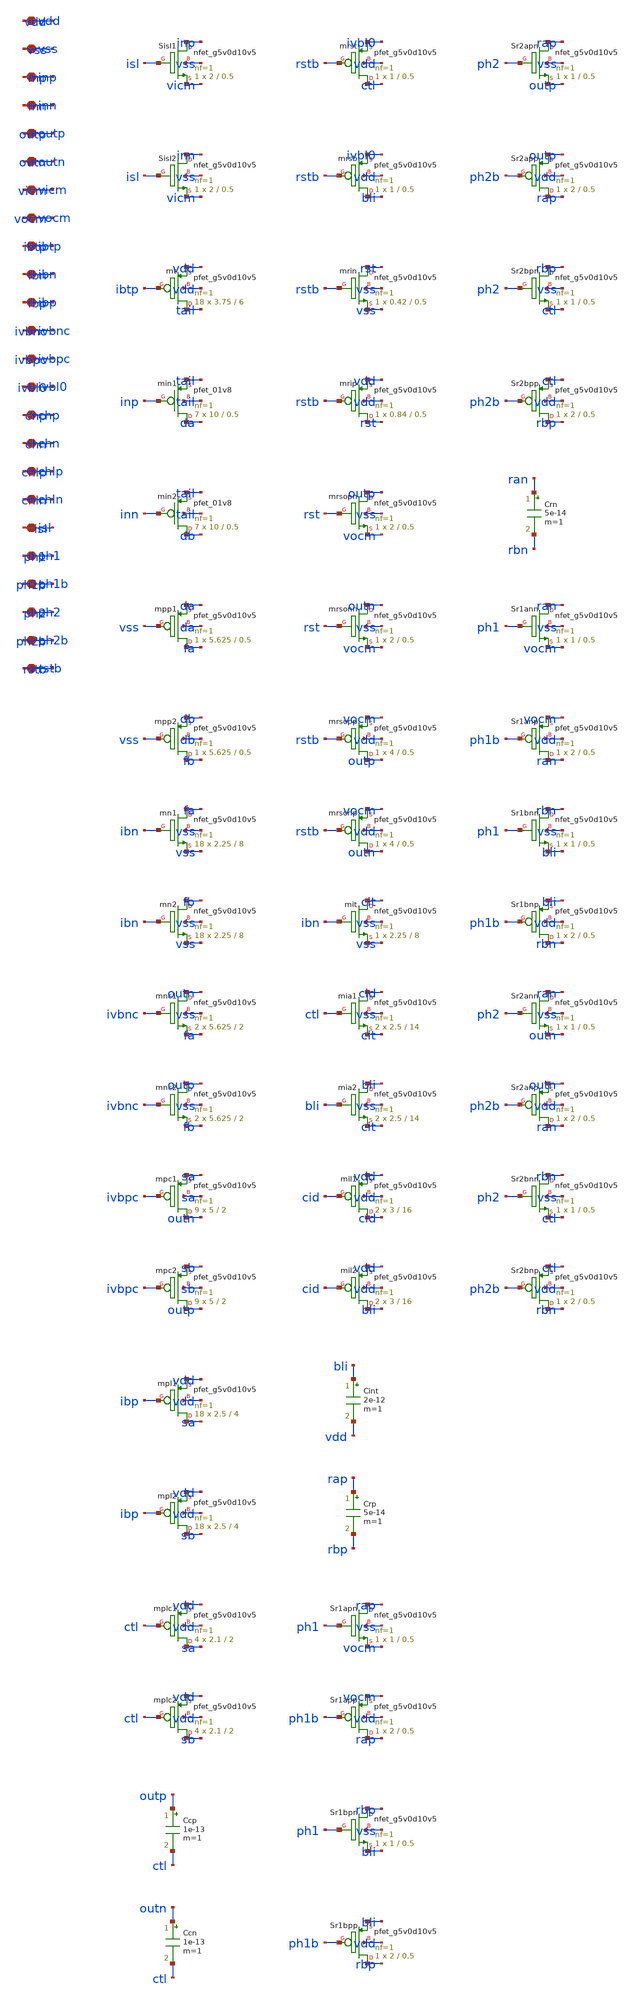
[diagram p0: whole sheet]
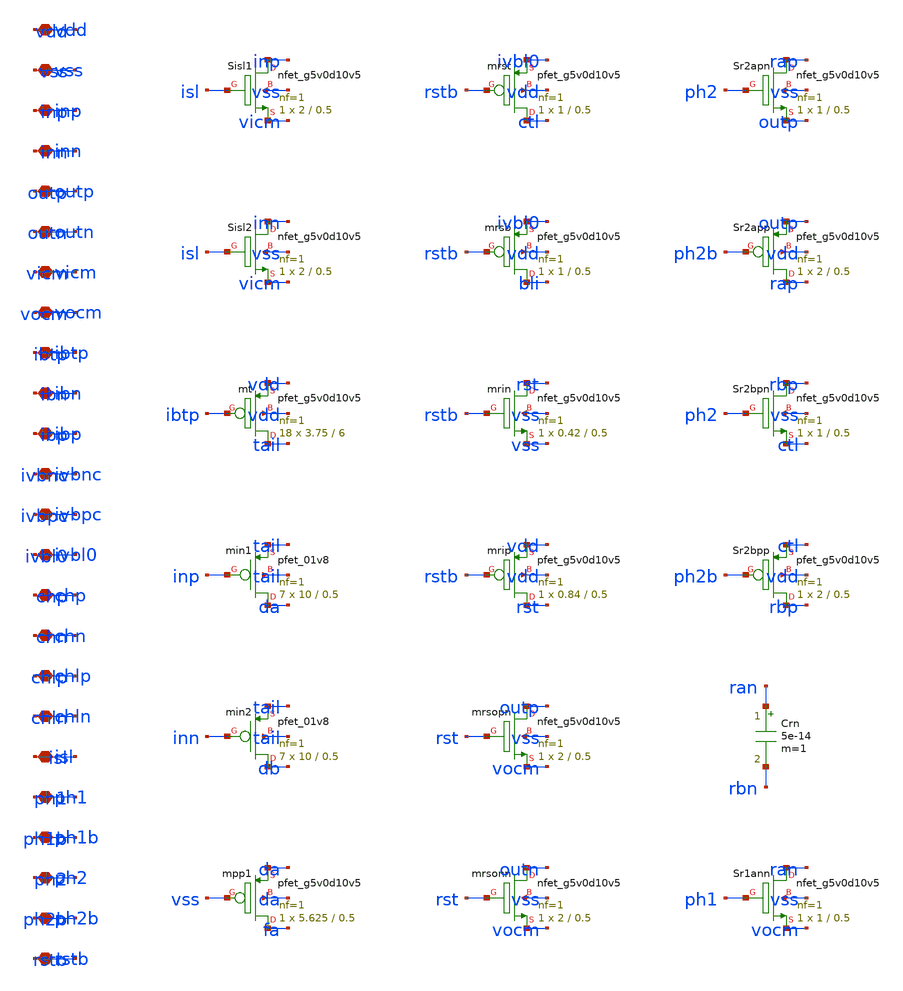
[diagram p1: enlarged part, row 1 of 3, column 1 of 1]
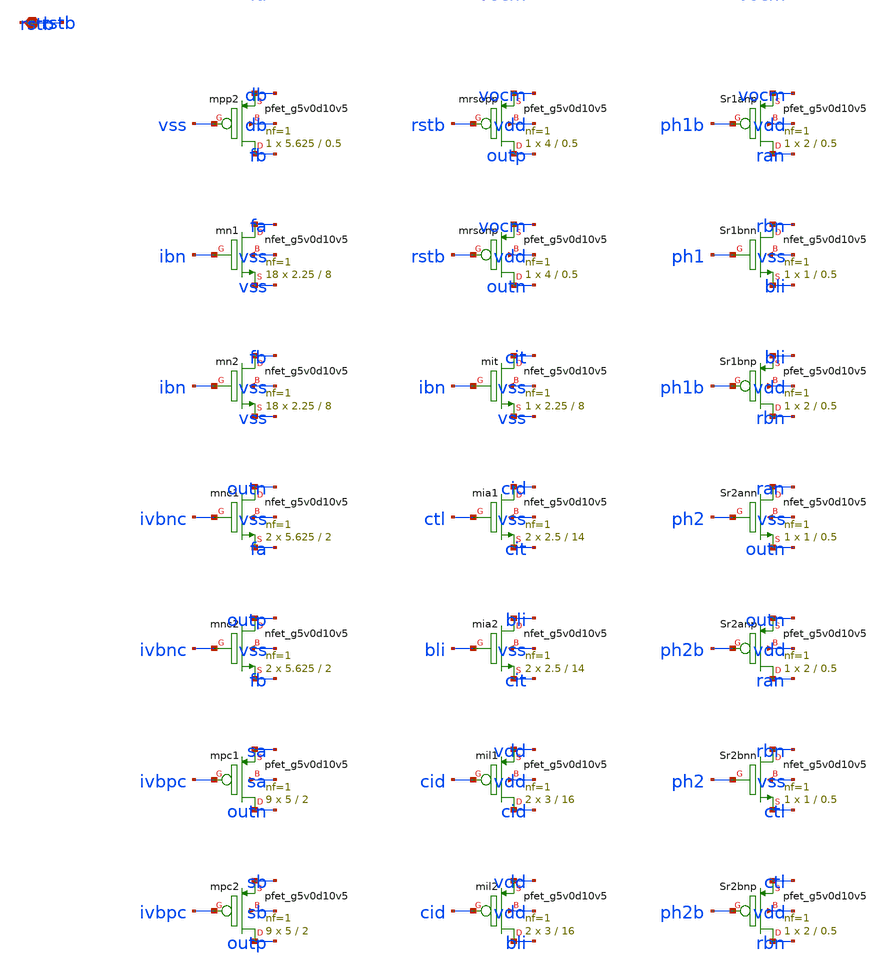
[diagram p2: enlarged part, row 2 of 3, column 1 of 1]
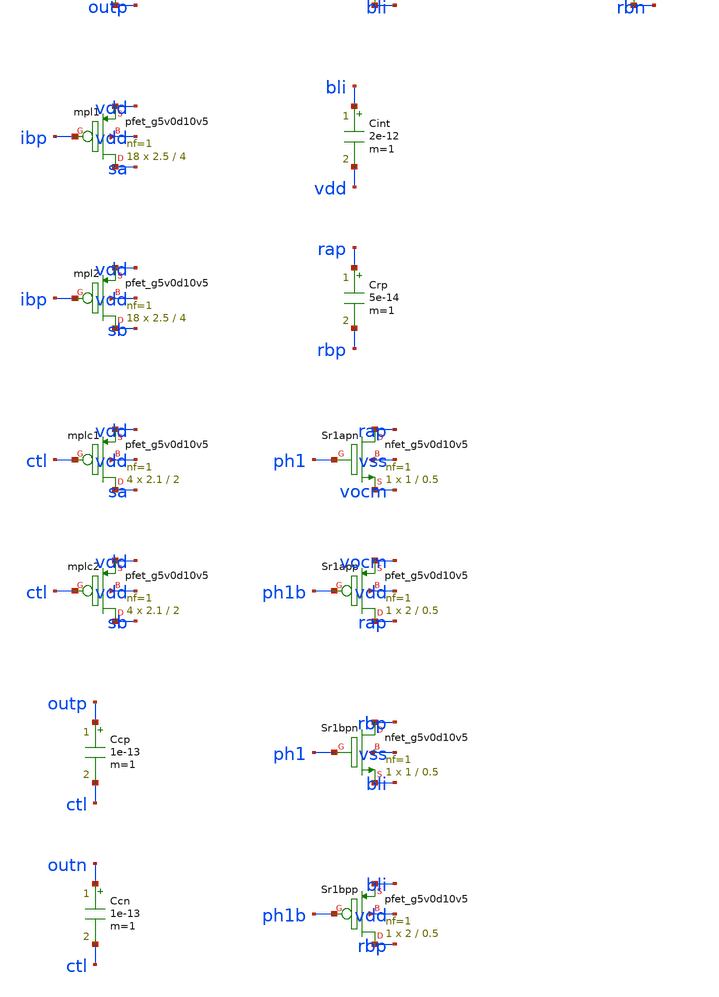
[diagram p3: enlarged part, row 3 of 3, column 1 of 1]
** sch_path: design/xschem/sch/ota2.sch
**.subckt ota2 vdd vss inp inn outp outn vicm vocm ibtp ibn ibp ivbnc ivbpc ivbl0 chp chn chlp chln
*+ isl ph1 ph1b ph2 ph2b rstb
*.iopin vdd
*.iopin vss
*.iopin inp
*.iopin inn
*.iopin outp
*.iopin outn
*.iopin vicm
*.iopin vocm
*.iopin ibtp
*.iopin ibn
*.iopin ibp
*.iopin ivbnc
*.iopin ivbpc
*.iopin ivbl0
*.iopin chp
*.iopin chn
*.iopin chlp
*.iopin chln
*.iopin isl
*.iopin ph1
*.iopin ph1b
*.iopin ph2
*.iopin ph2b
*.iopin rstb
XSisl1 inp isl vicm vss sky130_fd_pr__nfet_g5v0d10v5 L=0.5 W=2 nf=1 ad='int((1 + 1)/2) * 2 / 1 * 0.29'
+ as='int((1 + 2)/2) * 2 / 1 * 0.29' pd='2*int((1 + 1)/2) * (2 / 1 + 0.29)' ps='2*int((1 + 2)/2) * (2 / 1 + 0.29)'
+ nrd='0.29 / 2 ' nrs='0.29 / 2 ' sa=0 sb=0 sd=0 mult=1 m=1
XSisl2 inn isl vicm vss sky130_fd_pr__nfet_g5v0d10v5 L=0.5 W=2 nf=1 ad='int((1 + 1)/2) * 2 / 1 * 0.29'
+ as='int((1 + 2)/2) * 2 / 1 * 0.29' pd='2*int((1 + 1)/2) * (2 / 1 + 0.29)' ps='2*int((1 + 2)/2) * (2 / 1 + 0.29)'
+ nrd='0.29 / 2 ' nrs='0.29 / 2 ' sa=0 sb=0 sd=0 mult=1 m=1
Xmt tail ibtp vdd vdd sky130_fd_pr__pfet_g5v0d10v5 L=6 W=3.75 nf=1 ad='int((1 + 1)/2) * 3.75 / 1 * 0.29'
+ as='int((1 + 2)/2) * 3.75 / 1 * 0.29' pd='2*int((1 + 1)/2) * (3.75 / 1 + 0.29)' ps='2*int((1 + 2)/2) * (3.75 / 1 + 0.29)'
+ nrd='0.29 / 3.75 ' nrs='0.29 / 3.75 ' sa=0 sb=0 sd=0 mult=18 m=18
Xmin1 da inp tail tail sky130_fd_pr__pfet_01v8 L=0.5 W=10 nf=1 ad='int((nf+1)/2) * W/nf * 0.29' as='int((nf+2)/2) * W/nf * 0.29'
+ pd='2*int((nf+1)/2) * (W/nf + 0.29)' ps='2*int((nf+2)/2) * (W/nf + 0.29)' nrd='0.29 / W' nrs='0.29 / W'
+ sa=0 sb=0 sd=0 mult=7 m=7
Xmin2 db inn tail tail sky130_fd_pr__pfet_01v8 L=0.5 W=10 nf=1 ad='int((nf+1)/2) * W/nf * 0.29' as='int((nf+2)/2) * W/nf * 0.29'
+ pd='2*int((nf+1)/2) * (W/nf + 0.29)' ps='2*int((nf+2)/2) * (W/nf + 0.29)' nrd='0.29 / W' nrs='0.29 / W'
+ sa=0 sb=0 sd=0 mult=7 m=7
Xmpp1 fa vss da da sky130_fd_pr__pfet_g5v0d10v5 L=0.5 W=5.625 nf=1 ad='int((1 + 1)/2) * 5.625 / 1 * 0.29'
+ as='int((1 + 2)/2) * 5.625 / 1 * 0.29' pd='2*int((1 + 1)/2) * (5.625 / 1 + 0.29)' ps='2*int((1 + 2)/2) * (5.625 / 1 + 0.29)'
+ nrd='0.29 / 5.625 ' nrs='0.29 / 5.625 ' sa=0 sb=0 sd=0 mult=1 m=1
Xmpp2 fb vss db db sky130_fd_pr__pfet_g5v0d10v5 L=0.5 W=5.625 nf=1 ad='int((1 + 1)/2) * 5.625 / 1 * 0.29'
+ as='int((1 + 2)/2) * 5.625 / 1 * 0.29' pd='2*int((1 + 1)/2) * (5.625 / 1 + 0.29)' ps='2*int((1 + 2)/2) * (5.625 / 1 + 0.29)'
+ nrd='0.29 / 5.625 ' nrs='0.29 / 5.625 ' sa=0 sb=0 sd=0 mult=1 m=1
Xmn1 fa ibn vss vss sky130_fd_pr__nfet_g5v0d10v5 L=8 W=2.25 nf=1 ad='int((1 + 1)/2) * 2.25 / 1 * 0.29'
+ as='int((1 + 2)/2) * 2.25 / 1 * 0.29' pd='2*int((1 + 1)/2) * (2.25 / 1 + 0.29)' ps='2*int((1 + 2)/2) * (2.25 / 1 + 0.29)'
+ nrd='0.29 / 2.25 ' nrs='0.29 / 2.25 ' sa=0 sb=0 sd=0 mult=18 m=18
Xmn2 fb ibn vss vss sky130_fd_pr__nfet_g5v0d10v5 L=8 W=2.25 nf=1 ad='int((1 + 1)/2) * 2.25 / 1 * 0.29'
+ as='int((1 + 2)/2) * 2.25 / 1 * 0.29' pd='2*int((1 + 1)/2) * (2.25 / 1 + 0.29)' ps='2*int((1 + 2)/2) * (2.25 / 1 + 0.29)'
+ nrd='0.29 / 2.25 ' nrs='0.29 / 2.25 ' sa=0 sb=0 sd=0 mult=18 m=18
Xmnc1 outn ivbnc fa vss sky130_fd_pr__nfet_g5v0d10v5 L=2 W=5.625 nf=1 ad='int((1 + 1)/2) * 5.625 / 1 * 0.29'
+ as='int((1 + 2)/2) * 5.625 / 1 * 0.29' pd='2*int((1 + 1)/2) * (5.625 / 1 + 0.29)' ps='2*int((1 + 2)/2) * (5.625 / 1 + 0.29)'
+ nrd='0.29 / 5.625 ' nrs='0.29 / 5.625 ' sa=0 sb=0 sd=0 mult=2 m=2
Xmnc2 outp ivbnc fb vss sky130_fd_pr__nfet_g5v0d10v5 L=2 W=5.625 nf=1 ad='int((1 + 1)/2) * 5.625 / 1 * 0.29'
+ as='int((1 + 2)/2) * 5.625 / 1 * 0.29' pd='2*int((1 + 1)/2) * (5.625 / 1 + 0.29)' ps='2*int((1 + 2)/2) * (5.625 / 1 + 0.29)'
+ nrd='0.29 / 5.625 ' nrs='0.29 / 5.625 ' sa=0 sb=0 sd=0 mult=2 m=2
Xmpc1 outn ivbpc sa sa sky130_fd_pr__pfet_g5v0d10v5 L=2 W=5 nf=1 ad='int((1 + 1)/2) * 5 / 1 * 0.29' as='int((1 + 2)/2) * 5 / 1 * 0.29'
+ pd='2*int((1 + 1)/2) * (5 / 1 + 0.29)' ps='2*int((1 + 2)/2) * (5 / 1 + 0.29)' nrd='0.29 / 5 ' nrs='0.29 / 5 '
+ sa=0 sb=0 sd=0 mult=9 m=9
Xmpc2 outp ivbpc sb sb sky130_fd_pr__pfet_g5v0d10v5 L=2 W=5 nf=1 ad='int((1 + 1)/2) * 5 / 1 * 0.29' as='int((1 + 2)/2) * 5 / 1 * 0.29'
+ pd='2*int((1 + 1)/2) * (5 / 1 + 0.29)' ps='2*int((1 + 2)/2) * (5 / 1 + 0.29)' nrd='0.29 / 5 ' nrs='0.29 / 5 '
+ sa=0 sb=0 sd=0 mult=9 m=9
Xmpl1 sa ibp vdd vdd sky130_fd_pr__pfet_g5v0d10v5 L=4 W=2.5 nf=1 ad='int((1 + 1)/2) * 2.5 / 1 * 0.29'
+ as='int((1 + 2)/2) * 2.5 / 1 * 0.29' pd='2*int((1 + 1)/2) * (2.5 / 1 + 0.29)' ps='2*int((1 + 2)/2) * (2.5 / 1 + 0.29)'
+ nrd='0.29 / 2.5 ' nrs='0.29 / 2.5 ' sa=0 sb=0 sd=0 mult=18 m=18
Xmpl2 sb ibp vdd vdd sky130_fd_pr__pfet_g5v0d10v5 L=4 W=2.5 nf=1 ad='int((1 + 1)/2) * 2.5 / 1 * 0.29'
+ as='int((1 + 2)/2) * 2.5 / 1 * 0.29' pd='2*int((1 + 1)/2) * (2.5 / 1 + 0.29)' ps='2*int((1 + 2)/2) * (2.5 / 1 + 0.29)'
+ nrd='0.29 / 2.5 ' nrs='0.29 / 2.5 ' sa=0 sb=0 sd=0 mult=18 m=18
Xmplc1 sa ctl vdd vdd sky130_fd_pr__pfet_g5v0d10v5 L=2 W=2.1 nf=1 ad='int((1 + 1)/2) * 2.1 / 1 * 0.29'
+ as='int((1 + 2)/2) * 2.1 / 1 * 0.29' pd='2*int((1 + 1)/2) * (2.1 / 1 + 0.29)' ps='2*int((1 + 2)/2) * (2.1 / 1 + 0.29)'
+ nrd='0.29 / 2.1 ' nrs='0.29 / 2.1 ' sa=0 sb=0 sd=0 mult=4 m=4
Xmplc2 sb ctl vdd vdd sky130_fd_pr__pfet_g5v0d10v5 L=2 W=2.1 nf=1 ad='int((1 + 1)/2) * 2.1 / 1 * 0.29'
+ as='int((1 + 2)/2) * 2.1 / 1 * 0.29' pd='2*int((1 + 1)/2) * (2.1 / 1 + 0.29)' ps='2*int((1 + 2)/2) * (2.1 / 1 + 0.29)'
+ nrd='0.29 / 2.1 ' nrs='0.29 / 2.1 ' sa=0 sb=0 sd=0 mult=4 m=4
Ccp outp ctl 1e-13 m=1
Ccn outn ctl 1e-13 m=1
Xmrst ctl rstb ivbl0 vdd sky130_fd_pr__pfet_g5v0d10v5 L=0.5 W=1 nf=1 ad='int((1 + 1)/2) * 1 / 1 * 0.29'
+ as='int((1 + 2)/2) * 1 / 1 * 0.29' pd='2*int((1 + 1)/2) * (1 / 1 + 0.29)' ps='2*int((1 + 2)/2) * (1 / 1 + 0.29)'
+ nrd='0.29 / 1 ' nrs='0.29 / 1 ' sa=0 sb=0 sd=0 mult=1 m=1
Xmrsb bli rstb ivbl0 vdd sky130_fd_pr__pfet_g5v0d10v5 L=0.5 W=1 nf=1 ad='int((1 + 1)/2) * 1 / 1 * 0.29'
+ as='int((1 + 2)/2) * 1 / 1 * 0.29' pd='2*int((1 + 1)/2) * (1 / 1 + 0.29)' ps='2*int((1 + 2)/2) * (1 / 1 + 0.29)'
+ nrd='0.29 / 1 ' nrs='0.29 / 1 ' sa=0 sb=0 sd=0 mult=1 m=1
Xmrin rst rstb vss vss sky130_fd_pr__nfet_g5v0d10v5 L=0.5 W=0.42 nf=1 ad='int((1 + 1)/2) * 0.42 / 1 * 0.29'
+ as='int((1 + 2)/2) * 0.42 / 1 * 0.29' pd='2*int((1 + 1)/2) * (0.42 / 1 + 0.29)' ps='2*int((1 + 2)/2) * (0.42 / 1 + 0.29)'
+ nrd='0.29 / 0.42 ' nrs='0.29 / 0.42 ' sa=0 sb=0 sd=0 mult=1 m=1
Xmrip rst rstb vdd vdd sky130_fd_pr__pfet_g5v0d10v5 L=0.5 W=0.84 nf=1 ad='int((1 + 1)/2) * 0.84 / 1 * 0.29'
+ as='int((1 + 2)/2) * 0.84 / 1 * 0.29' pd='2*int((1 + 1)/2) * (0.84 / 1 + 0.29)' ps='2*int((1 + 2)/2) * (0.84 / 1 + 0.29)'
+ nrd='0.29 / 0.84 ' nrs='0.29 / 0.84 ' sa=0 sb=0 sd=0 mult=1 m=1
Xmrsopn outp rst vocm vss sky130_fd_pr__nfet_g5v0d10v5 L=0.5 W=2 nf=1 ad='int((1 + 1)/2) * 2 / 1 * 0.29'
+ as='int((1 + 2)/2) * 2 / 1 * 0.29' pd='2*int((1 + 1)/2) * (2 / 1 + 0.29)' ps='2*int((1 + 2)/2) * (2 / 1 + 0.29)'
+ nrd='0.29 / 2 ' nrs='0.29 / 2 ' sa=0 sb=0 sd=0 mult=1 m=1
Xmrsonn outn rst vocm vss sky130_fd_pr__nfet_g5v0d10v5 L=0.5 W=2 nf=1 ad='int((1 + 1)/2) * 2 / 1 * 0.29'
+ as='int((1 + 2)/2) * 2 / 1 * 0.29' pd='2*int((1 + 1)/2) * (2 / 1 + 0.29)' ps='2*int((1 + 2)/2) * (2 / 1 + 0.29)'
+ nrd='0.29 / 2 ' nrs='0.29 / 2 ' sa=0 sb=0 sd=0 mult=1 m=1
Xmrsopp outp rstb vocm vdd sky130_fd_pr__pfet_g5v0d10v5 L=0.5 W=4 nf=1 ad='int((1 + 1)/2) * 4 / 1 * 0.29'
+ as='int((1 + 2)/2) * 4 / 1 * 0.29' pd='2*int((1 + 1)/2) * (4 / 1 + 0.29)' ps='2*int((1 + 2)/2) * (4 / 1 + 0.29)'
+ nrd='0.29 / 4 ' nrs='0.29 / 4 ' sa=0 sb=0 sd=0 mult=1 m=1
Xmrsonp outn rstb vocm vdd sky130_fd_pr__pfet_g5v0d10v5 L=0.5 W=4 nf=1 ad='int((1 + 1)/2) * 4 / 1 * 0.29'
+ as='int((1 + 2)/2) * 4 / 1 * 0.29' pd='2*int((1 + 1)/2) * (4 / 1 + 0.29)' ps='2*int((1 + 2)/2) * (4 / 1 + 0.29)'
+ nrd='0.29 / 4 ' nrs='0.29 / 4 ' sa=0 sb=0 sd=0 mult=1 m=1
Xmit cit ibn vss vss sky130_fd_pr__nfet_g5v0d10v5 L=8 W=2.25 nf=1 ad='int((1 + 1)/2) * 2.25 / 1 * 0.29'
+ as='int((1 + 2)/2) * 2.25 / 1 * 0.29' pd='2*int((1 + 1)/2) * (2.25 / 1 + 0.29)' ps='2*int((1 + 2)/2) * (2.25 / 1 + 0.29)'
+ nrd='0.29 / 2.25 ' nrs='0.29 / 2.25 ' sa=0 sb=0 sd=0 mult=1 m=1
Xmia1 cid ctl cit vss sky130_fd_pr__nfet_g5v0d10v5 L=14 W=2.5 nf=1 ad='int((1 + 1)/2) * 2.5 / 1 * 0.29'
+ as='int((1 + 2)/2) * 2.5 / 1 * 0.29' pd='2*int((1 + 1)/2) * (2.5 / 1 + 0.29)' ps='2*int((1 + 2)/2) * (2.5 / 1 + 0.29)'
+ nrd='0.29 / 2.5 ' nrs='0.29 / 2.5 ' sa=0 sb=0 sd=0 mult=2 m=2
Xmia2 bli bli cit vss sky130_fd_pr__nfet_g5v0d10v5 L=14 W=2.5 nf=1 ad='int((1 + 1)/2) * 2.5 / 1 * 0.29'
+ as='int((1 + 2)/2) * 2.5 / 1 * 0.29' pd='2*int((1 + 1)/2) * (2.5 / 1 + 0.29)' ps='2*int((1 + 2)/2) * (2.5 / 1 + 0.29)'
+ nrd='0.29 / 2.5 ' nrs='0.29 / 2.5 ' sa=0 sb=0 sd=0 mult=2 m=2
Xmil1 cid cid vdd vdd sky130_fd_pr__pfet_g5v0d10v5 L=16 W=3 nf=1 ad='int((1 + 1)/2) * 3 / 1 * 0.29' as='int((1 + 2)/2) * 3 / 1 * 0.29'
+ pd='2*int((1 + 1)/2) * (3 / 1 + 0.29)' ps='2*int((1 + 2)/2) * (3 / 1 + 0.29)' nrd='0.29 / 3 ' nrs='0.29 / 3 '
+ sa=0 sb=0 sd=0 mult=2 m=2
Xmil2 bli cid vdd vdd sky130_fd_pr__pfet_g5v0d10v5 L=16 W=3 nf=1 ad='int((1 + 1)/2) * 3 / 1 * 0.29' as='int((1 + 2)/2) * 3 / 1 * 0.29'
+ pd='2*int((1 + 1)/2) * (3 / 1 + 0.29)' ps='2*int((1 + 2)/2) * (3 / 1 + 0.29)' nrd='0.29 / 3 ' nrs='0.29 / 3 '
+ sa=0 sb=0 sd=0 mult=2 m=2
Cint bli vdd 2e-12 m=1
Crp rap rbp 5e-14 m=1
XSr1apn rap ph1 vocm vss sky130_fd_pr__nfet_g5v0d10v5 L=0.5 W=1 nf=1 ad='int((1 + 1)/2) * 1 / 1 * 0.29'
+ as='int((1 + 2)/2) * 1 / 1 * 0.29' pd='2*int((1 + 1)/2) * (1 / 1 + 0.29)' ps='2*int((1 + 2)/2) * (1 / 1 + 0.29)'
+ nrd='0.29 / 1 ' nrs='0.29 / 1 ' sa=0 sb=0 sd=0 mult=1 m=1
XSr1app rap ph1b vocm vdd sky130_fd_pr__pfet_g5v0d10v5 L=0.5 W=2 nf=1 ad='int((1 + 1)/2) * 2 / 1 * 0.29'
+ as='int((1 + 2)/2) * 2 / 1 * 0.29' pd='2*int((1 + 1)/2) * (2 / 1 + 0.29)' ps='2*int((1 + 2)/2) * (2 / 1 + 0.29)'
+ nrd='0.29 / 2 ' nrs='0.29 / 2 ' sa=0 sb=0 sd=0 mult=1 m=1
XSr1bpn rbp ph1 bli vss sky130_fd_pr__nfet_g5v0d10v5 L=0.5 W=1 nf=1 ad='int((1 + 1)/2) * 1 / 1 * 0.29'
+ as='int((1 + 2)/2) * 1 / 1 * 0.29' pd='2*int((1 + 1)/2) * (1 / 1 + 0.29)' ps='2*int((1 + 2)/2) * (1 / 1 + 0.29)'
+ nrd='0.29 / 1 ' nrs='0.29 / 1 ' sa=0 sb=0 sd=0 mult=1 m=1
XSr1bpp rbp ph1b bli vdd sky130_fd_pr__pfet_g5v0d10v5 L=0.5 W=2 nf=1 ad='int((1 + 1)/2) * 2 / 1 * 0.29'
+ as='int((1 + 2)/2) * 2 / 1 * 0.29' pd='2*int((1 + 1)/2) * (2 / 1 + 0.29)' ps='2*int((1 + 2)/2) * (2 / 1 + 0.29)'
+ nrd='0.29 / 2 ' nrs='0.29 / 2 ' sa=0 sb=0 sd=0 mult=1 m=1
XSr2apn rap ph2 outp vss sky130_fd_pr__nfet_g5v0d10v5 L=0.5 W=1 nf=1 ad='int((1 + 1)/2) * 1 / 1 * 0.29'
+ as='int((1 + 2)/2) * 1 / 1 * 0.29' pd='2*int((1 + 1)/2) * (1 / 1 + 0.29)' ps='2*int((1 + 2)/2) * (1 / 1 + 0.29)'
+ nrd='0.29 / 1 ' nrs='0.29 / 1 ' sa=0 sb=0 sd=0 mult=1 m=1
XSr2app rap ph2b outp vdd sky130_fd_pr__pfet_g5v0d10v5 L=0.5 W=2 nf=1 ad='int((1 + 1)/2) * 2 / 1 * 0.29'
+ as='int((1 + 2)/2) * 2 / 1 * 0.29' pd='2*int((1 + 1)/2) * (2 / 1 + 0.29)' ps='2*int((1 + 2)/2) * (2 / 1 + 0.29)'
+ nrd='0.29 / 2 ' nrs='0.29 / 2 ' sa=0 sb=0 sd=0 mult=1 m=1
XSr2bpn rbp ph2 ctl vss sky130_fd_pr__nfet_g5v0d10v5 L=0.5 W=1 nf=1 ad='int((1 + 1)/2) * 1 / 1 * 0.29'
+ as='int((1 + 2)/2) * 1 / 1 * 0.29' pd='2*int((1 + 1)/2) * (1 / 1 + 0.29)' ps='2*int((1 + 2)/2) * (1 / 1 + 0.29)'
+ nrd='0.29 / 1 ' nrs='0.29 / 1 ' sa=0 sb=0 sd=0 mult=1 m=1
XSr2bpp rbp ph2b ctl vdd sky130_fd_pr__pfet_g5v0d10v5 L=0.5 W=2 nf=1 ad='int((1 + 1)/2) * 2 / 1 * 0.29'
+ as='int((1 + 2)/2) * 2 / 1 * 0.29' pd='2*int((1 + 1)/2) * (2 / 1 + 0.29)' ps='2*int((1 + 2)/2) * (2 / 1 + 0.29)'
+ nrd='0.29 / 2 ' nrs='0.29 / 2 ' sa=0 sb=0 sd=0 mult=1 m=1
Crn ran rbn 5e-14 m=1
XSr1ann ran ph1 vocm vss sky130_fd_pr__nfet_g5v0d10v5 L=0.5 W=1 nf=1 ad='int((1 + 1)/2) * 1 / 1 * 0.29'
+ as='int((1 + 2)/2) * 1 / 1 * 0.29' pd='2*int((1 + 1)/2) * (1 / 1 + 0.29)' ps='2*int((1 + 2)/2) * (1 / 1 + 0.29)'
+ nrd='0.29 / 1 ' nrs='0.29 / 1 ' sa=0 sb=0 sd=0 mult=1 m=1
XSr1anp ran ph1b vocm vdd sky130_fd_pr__pfet_g5v0d10v5 L=0.5 W=2 nf=1 ad='int((1 + 1)/2) * 2 / 1 * 0.29'
+ as='int((1 + 2)/2) * 2 / 1 * 0.29' pd='2*int((1 + 1)/2) * (2 / 1 + 0.29)' ps='2*int((1 + 2)/2) * (2 / 1 + 0.29)'
+ nrd='0.29 / 2 ' nrs='0.29 / 2 ' sa=0 sb=0 sd=0 mult=1 m=1
XSr1bnn rbn ph1 bli vss sky130_fd_pr__nfet_g5v0d10v5 L=0.5 W=1 nf=1 ad='int((1 + 1)/2) * 1 / 1 * 0.29'
+ as='int((1 + 2)/2) * 1 / 1 * 0.29' pd='2*int((1 + 1)/2) * (1 / 1 + 0.29)' ps='2*int((1 + 2)/2) * (1 / 1 + 0.29)'
+ nrd='0.29 / 1 ' nrs='0.29 / 1 ' sa=0 sb=0 sd=0 mult=1 m=1
XSr1bnp rbn ph1b bli vdd sky130_fd_pr__pfet_g5v0d10v5 L=0.5 W=2 nf=1 ad='int((1 + 1)/2) * 2 / 1 * 0.29'
+ as='int((1 + 2)/2) * 2 / 1 * 0.29' pd='2*int((1 + 1)/2) * (2 / 1 + 0.29)' ps='2*int((1 + 2)/2) * (2 / 1 + 0.29)'
+ nrd='0.29 / 2 ' nrs='0.29 / 2 ' sa=0 sb=0 sd=0 mult=1 m=1
XSr2ann ran ph2 outn vss sky130_fd_pr__nfet_g5v0d10v5 L=0.5 W=1 nf=1 ad='int((1 + 1)/2) * 1 / 1 * 0.29'
+ as='int((1 + 2)/2) * 1 / 1 * 0.29' pd='2*int((1 + 1)/2) * (1 / 1 + 0.29)' ps='2*int((1 + 2)/2) * (1 / 1 + 0.29)'
+ nrd='0.29 / 1 ' nrs='0.29 / 1 ' sa=0 sb=0 sd=0 mult=1 m=1
XSr2anp ran ph2b outn vdd sky130_fd_pr__pfet_g5v0d10v5 L=0.5 W=2 nf=1 ad='int((1 + 1)/2) * 2 / 1 * 0.29'
+ as='int((1 + 2)/2) * 2 / 1 * 0.29' pd='2*int((1 + 1)/2) * (2 / 1 + 0.29)' ps='2*int((1 + 2)/2) * (2 / 1 + 0.29)'
+ nrd='0.29 / 2 ' nrs='0.29 / 2 ' sa=0 sb=0 sd=0 mult=1 m=1
XSr2bnn rbn ph2 ctl vss sky130_fd_pr__nfet_g5v0d10v5 L=0.5 W=1 nf=1 ad='int((1 + 1)/2) * 1 / 1 * 0.29'
+ as='int((1 + 2)/2) * 1 / 1 * 0.29' pd='2*int((1 + 1)/2) * (1 / 1 + 0.29)' ps='2*int((1 + 2)/2) * (1 / 1 + 0.29)'
+ nrd='0.29 / 1 ' nrs='0.29 / 1 ' sa=0 sb=0 sd=0 mult=1 m=1
XSr2bnp rbn ph2b ctl vdd sky130_fd_pr__pfet_g5v0d10v5 L=0.5 W=2 nf=1 ad='int((1 + 1)/2) * 2 / 1 * 0.29'
+ as='int((1 + 2)/2) * 2 / 1 * 0.29' pd='2*int((1 + 1)/2) * (2 / 1 + 0.29)' ps='2*int((1 + 2)/2) * (2 / 1 + 0.29)'
+ nrd='0.29 / 2 ' nrs='0.29 / 2 ' sa=0 sb=0 sd=0 mult=1 m=1
**.ends
.end
